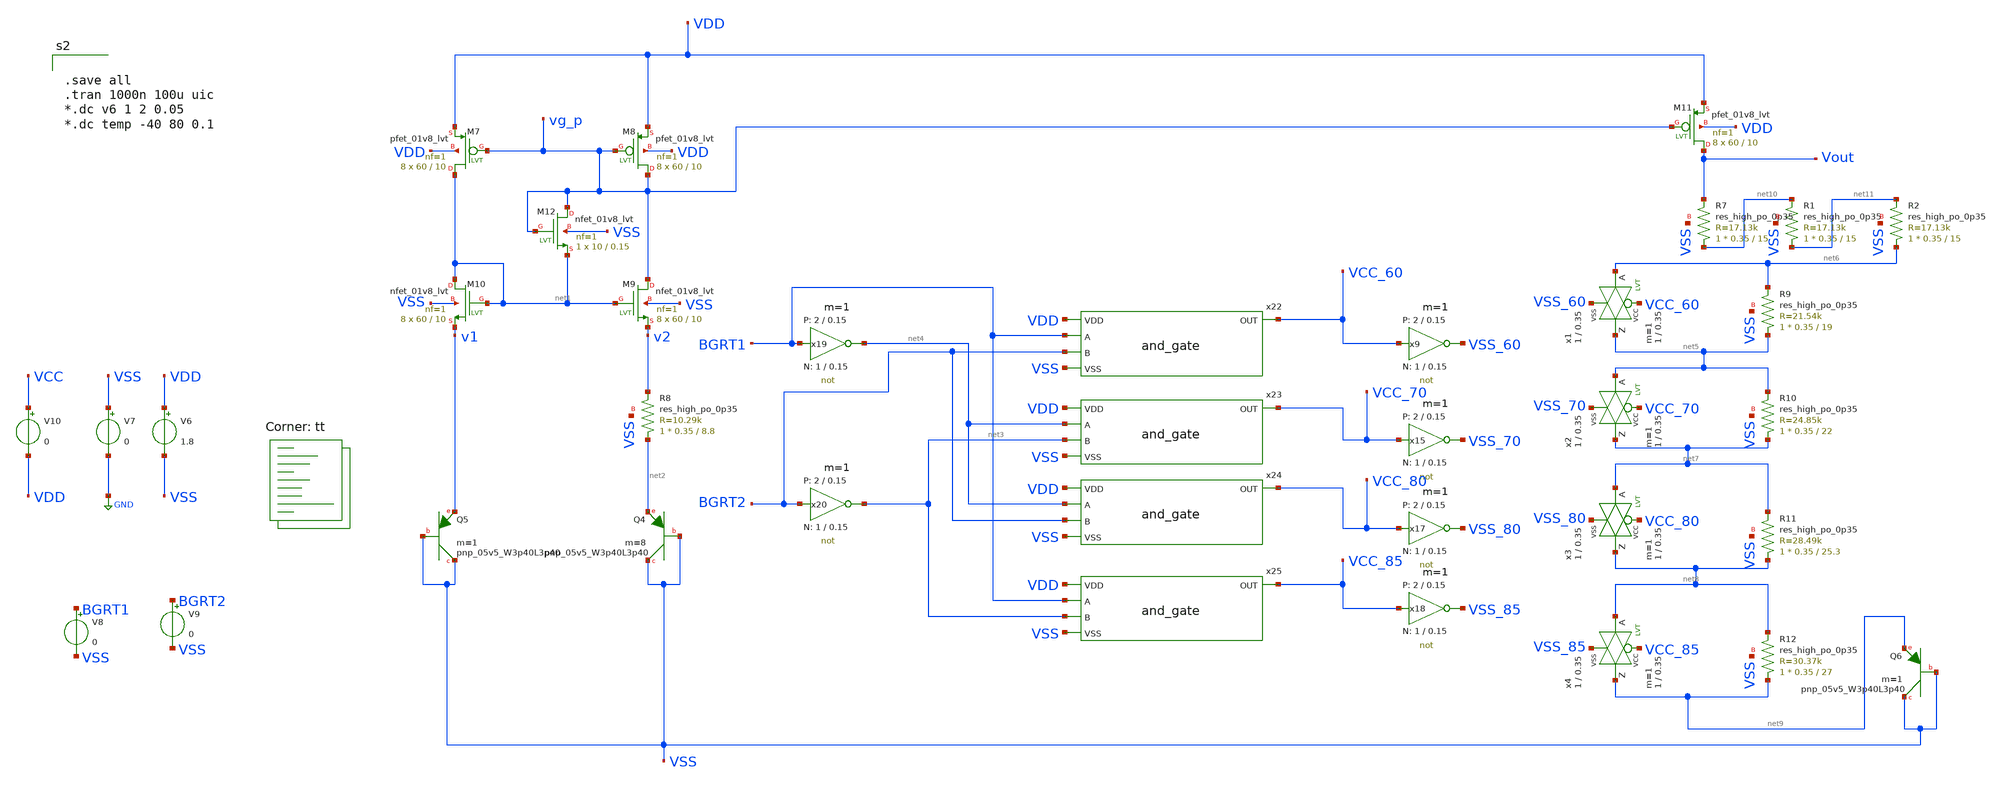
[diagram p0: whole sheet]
** sch_path: xschem/bandgap_testbench.sch
**.subckt bandgap_testbench
XM7 net1 vg_p VDD VDD sky130_fd_pr__pfet_01v8_lvt L=10 W=60 nf=1 ad='int((nf+1)/2) * W/nf * 0.29' as='int((nf+2)/2) * W/nf * 0.29'
+ pd='2*int((nf+1)/2) * (W/nf + 0.29)' ps='2*int((nf+2)/2) * (W/nf + 0.29)' nrd='0.29 / W' nrs='0.29 / W'
+ sa=0 sb=0 sd=0 mult=8 m=8
XM8 vg_p vg_p VDD VDD sky130_fd_pr__pfet_01v8_lvt L=10 W=60 nf=1 ad='int((nf+1)/2) * W/nf * 0.29' as='int((nf+2)/2) * W/nf * 0.29'
+ pd='2*int((nf+1)/2) * (W/nf + 0.29)' ps='2*int((nf+2)/2) * (W/nf + 0.29)' nrd='0.29 / W' nrs='0.29 / W'
+ sa=0 sb=0 sd=0 mult=8 m=8
XM9 vg_p net1 v2 VSS sky130_fd_pr__nfet_01v8_lvt L=10 W=60 nf=1 ad='int((nf+1)/2) * W/nf * 0.29' as='int((nf+2)/2) * W/nf * 0.29'
+ pd='2*int((nf+1)/2) * (W/nf + 0.29)' ps='2*int((nf+2)/2) * (W/nf + 0.29)' nrd='0.29 / W' nrs='0.29 / W'
+ sa=0 sb=0 sd=0 mult=8 m=8
XM10 net1 net1 v1 VSS sky130_fd_pr__nfet_01v8_lvt L=10 W=60 nf=1 ad='int((nf+1)/2) * W/nf * 0.29' as='int((nf+2)/2) * W/nf * 0.29'
+ pd='2*int((nf+1)/2) * (W/nf + 0.29)' ps='2*int((nf+2)/2) * (W/nf + 0.29)' nrd='0.29 / W' nrs='0.29 / W'
+ sa=0 sb=0 sd=0 mult=8 m=8
XQ4 VSS VSS net2 sky130_fd_pr__pnp_05v5_W3p40L3p40 m=8
XQ5 VSS VSS v1 sky130_fd_pr__pnp_05v5_W3p40L3p40 m=1
V6 VDD VSS 1.8
V7 VSS GND 0
V8 BGRT1 VSS 0
V9 BGRT2 VSS 0
XM11 Vout vg_p VDD VDD sky130_fd_pr__pfet_01v8_lvt L=10 W=60 nf=1 ad='int((nf+1)/2) * W/nf * 0.29' as='int((nf+2)/2) * W/nf * 0.29'
+ pd='2*int((nf+1)/2) * (W/nf + 0.29)' ps='2*int((nf+2)/2) * (W/nf + 0.29)' nrd='0.29 / W' nrs='0.29 / W'
+ sa=0 sb=0 sd=0 mult=8 m=8
x9 VSS_60 VCC_60 VCC VSS not W_N=1 L_N=0.15 W_P=2 L_P=0.15 m=1
x15 VSS_70 VCC_70 VCC VSS not W_N=1 L_N=0.15 W_P=2 L_P=0.15 m=1
x17 VSS_80 VCC_80 VCC VSS not W_N=1 L_N=0.15 W_P=2 L_P=0.15 m=1
x18 VSS_85 VCC_85 VCC VSS not W_N=1 L_N=0.15 W_P=2 L_P=0.15 m=1
x19 net4 BGRT1 VCC VSS not W_N=1 L_N=0.15 W_P=2 L_P=0.15 m=1
x20 net3 BGRT2 VCC VSS not W_N=1 L_N=0.15 W_P=2 L_P=0.15 m=1
XR7 net10 Vout VSS sky130_fd_pr__res_high_po_0p35 L=15 mult=1 m=1
XM12 vg_p vg_p net1 VSS sky130_fd_pr__nfet_01v8_lvt L=0.15 W=10 nf=1 ad='int((nf+1)/2) * W/nf * 0.29'
+ as='int((nf+2)/2) * W/nf * 0.29' pd='2*int((nf+1)/2) * (W/nf + 0.29)' ps='2*int((nf+2)/2) * (W/nf + 0.29)'
+ nrd='0.29 / W' nrs='0.29 / W' sa=0 sb=0 sd=0 mult=1 m=1
XR8 net2 v2 VSS sky130_fd_pr__res_high_po_0p35 L=8.8 mult=1 m=1
XR9 net5 net6 VSS sky130_fd_pr__res_high_po_0p35 L=19 mult=1 m=1
x22 VDD BGRT1 VCC_60 BGRT2 VSS and_gate
x23 VDD net4 VCC_70 net3 VSS and_gate
x24 VDD net4 VCC_80 BGRT2 VSS and_gate
x25 VDD BGRT1 VCC_85 net3 VSS and_gate
XR10 net7 net5 VSS sky130_fd_pr__res_high_po_0p35 L=22 mult=1 m=1
XR11 net8 net7 VSS sky130_fd_pr__res_high_po_0p35 L=25.3 mult=1 m=1
XR12 net9 net8 VSS sky130_fd_pr__res_high_po_0p35 L=27 mult=1 m=1
XQ6 VSS VSS net9 sky130_fd_pr__pnp_05v5_W3p40L3p40 m=1
V10 VCC VDD 0
x1 net5 net6 VCC_60 VSS_60 VCC VSS passgate_nlvt W_N=1 L_N=0.35 W_P=1 L_P=0.35 m=1
x2 net7 net5 VCC_70 VSS_70 VCC VSS passgate_nlvt W_N=1 L_N=0.35 W_P=1 L_P=0.35 m=1
x3 net8 net7 VCC_80 VSS_80 VCC VSS passgate_nlvt W_N=1 L_N=0.35 W_P=1 L_P=0.35 m=1
x4 net9 net8 VCC_85 VSS_85 VCC VSS passgate_nlvt W_N=1 L_N=0.35 W_P=1 L_P=0.35 m=1
XR1 net11 net10 VSS sky130_fd_pr__res_high_po_0p35 L=15 mult=1 m=1
XR2 net6 net11 VSS sky130_fd_pr__res_high_po_0p35 L=15 mult=1 m=1
**** begin user architecture code


.save all
.tran 1000n 100u uic
*.dc v6 1 2 0.05
*.dc temp -40 80 0.1


.lib $::SKYWATER_MODELS/sky130.lib.spice tt
**** end user architecture code
**.ends
.GLOBAL GND
.end
